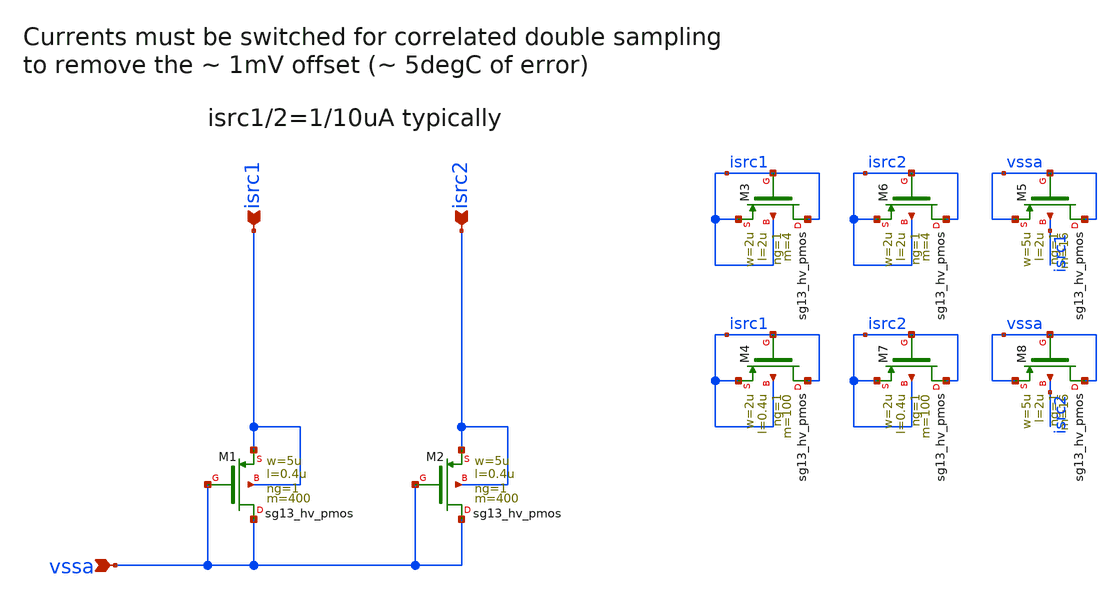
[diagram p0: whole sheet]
** sch_path: Schematics_Layout/sunrise_tsns_DTMOS/sunrise_tsns_DTMOS.sch
**.subckt sunrise_tsns_DTMOS isrc1 isrc2 vssa
*.ipin isrc1
*.ipin isrc2
*.ipin vssa
XM1 vssa vssa isrc1 isrc1 sg13_hv_pmos w=5u l=0.4u ng=1 m=400 mm_ok=1
XM2 vssa vssa isrc2 isrc2 sg13_hv_pmos w=5u l=0.4u ng=1 m=400 mm_ok=1
XM3 isrc1 isrc1 isrc1 isrc1 sg13_hv_pmos w=2u l=2u ng=1 m=4 mm_ok=1
XM4 isrc1 isrc1 isrc1 isrc1 sg13_hv_pmos w=2u l=0.4u ng=1 m=100 mm_ok=1
XM5 vssa vssa vssa isrc1 sg13_hv_pmos w=5u l=2u ng=1 m=16 mm_ok=1
XM6 isrc2 isrc2 isrc2 isrc2 sg13_hv_pmos w=2u l=2u ng=1 m=4 mm_ok=1
XM7 isrc2 isrc2 isrc2 isrc2 sg13_hv_pmos w=2u l=0.4u ng=1 m=100 mm_ok=1
XM8 vssa vssa vssa isrc2 sg13_hv_pmos w=5u l=2u ng=1 m=16 mm_ok=1
**.ends
.end
